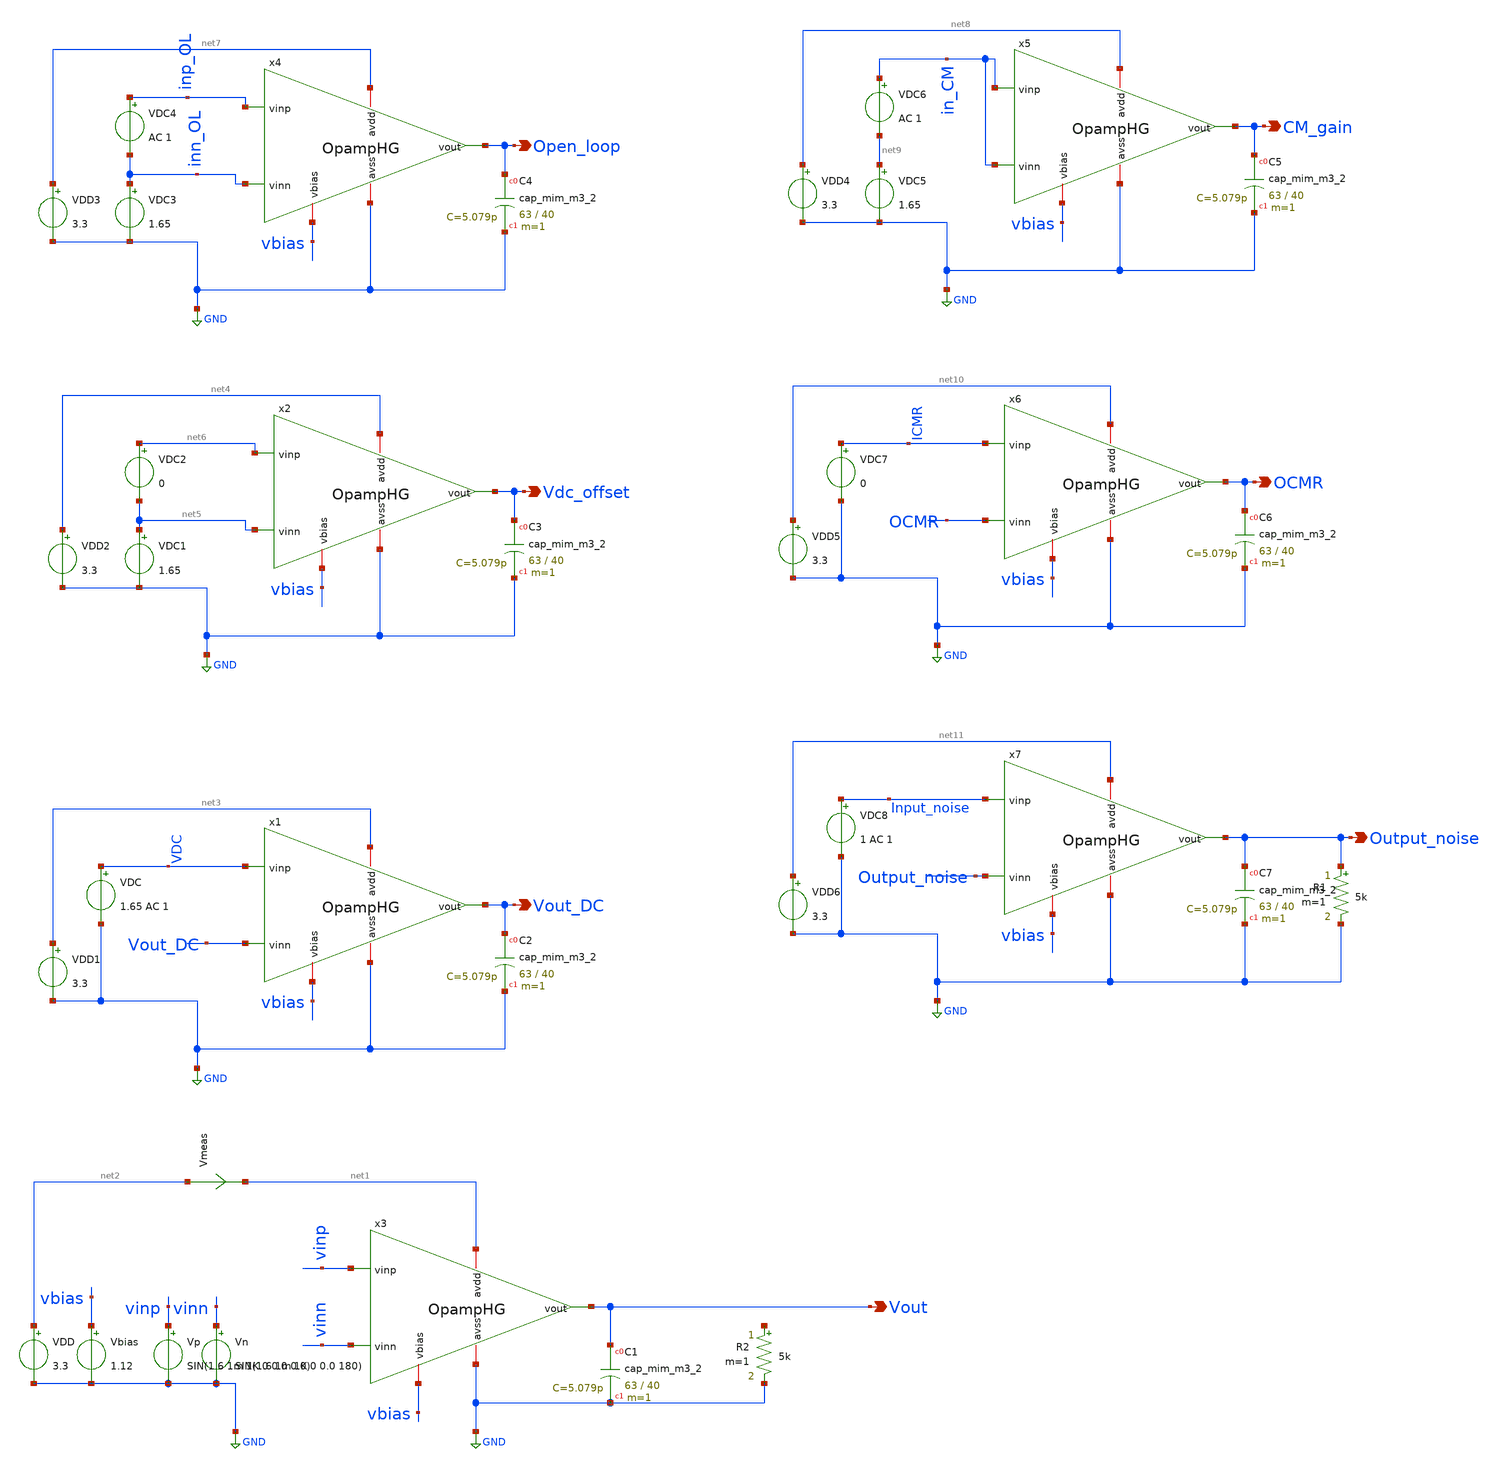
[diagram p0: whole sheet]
** sch_path: OpampHG_tb.sch
**.subckt OpampHG_tb Vout Vout_DC Vdc_offset Open_loop CM_gain OCMR Output_noise
*.opin Vout
*.opin Vout_DC
*.opin Vdc_offset
*.opin Open_loop
*.opin CM_gain
*.opin OCMR
*.opin Output_noise
Vp vinp GND SIN(1.6 1m 1K 0 0.0 0.0)
Vn vinn GND SIN(1.6 1m 1K 0 0.0 180)
VDD net2 GND 3.3
Vbias vbias GND 1.12
XC1 Vout GND sky130_fd_pr__cap_mim_m3_2 W=63 L=40 MF=1 m=1
x3 net1 GND vbias vinp vinn Vout OpampHG
x1 net3 GND vbias VDC Vout_DC Vout_DC OpampHG
VDD1 net3 GND 3.3
VDC VDC GND 1.65 AC 1
XC2 Vout_DC GND sky130_fd_pr__cap_mim_m3_2 W=63 L=40 MF=1 m=1
R1 Output_noise GND 5k m=1
x2 net4 GND vbias net6 net5 Vdc_offset OpampHG
VDD2 net4 GND 3.3
VDC1 net5 GND 1.65
XC3 Vdc_offset GND sky130_fd_pr__cap_mim_m3_2 W=63 L=40 MF=1 m=1
VDC2 net6 net5 0
x4 net7 GND vbias inp_OL inn_OL Open_loop OpampHG
VDD3 net7 GND 3.3
VDC3 inn_OL GND 1.65
XC4 Open_loop GND sky130_fd_pr__cap_mim_m3_2 W=63 L=40 MF=1 m=1
VDC4 inp_OL inn_OL AC 1
x5 net8 GND vbias in_CM in_CM CM_gain OpampHG
VDD4 net8 GND 3.3
VDC5 net9 GND 1.65
XC5 CM_gain GND sky130_fd_pr__cap_mim_m3_2 W=63 L=40 MF=1 m=1
VDC6 in_CM net9 AC 1
x6 net10 GND vbias ICMR OCMR OCMR OpampHG
VDD5 net10 GND 3.3
VDC7 ICMR GND 0
XC6 OCMR GND sky130_fd_pr__cap_mim_m3_2 W=63 L=40 MF=1 m=1
x7 net11 GND vbias Input_noise Output_noise Output_noise OpampHG
VDD6 net11 GND 3.3
VDC8 Input_noise GND 1 AC 1
XC7 Output_noise GND sky130_fd_pr__cap_mim_m3_2 W=63 L=40 MF=1 m=1
R2 net12 GND 5k m=1
Vmeas net2 net1 0
.save i(vmeas)
**** begin user architecture code


.lib /foss/pdks/sky130A/libs.tech/ngspice/sky130.lib.spice tt
.control

*****************dc analysis************
*dc VDC7 0 3.3 0.1
*plot v(OCMR) v(ICMR)
*dc VDC2 -5m 5m 1m
*plot v(Vdc_offset)


*****************AC analysis************
ac dec 20 1 1e10
let Open_Loop_Gain = v(Open_loop)/(v(inp_OL)-v(inn_OL))
let Common_mode_gain = v(CM_gain)/v(in_CM)
let Phase_Degree=180*cph(v(Open_loop)/(v(inp_OL)-v(inn_OL)))/pi
let CMRR=Open_Loop_Gain/Common_mode_gain
plot v(Vout_DC)
plot db(Open_Loop_Gain)
plot Phase_Degree
plot db(CMRR)
write Output_AC.raw

****************Transient Analysis******
*tran 0.1m 5m
*plot v(vinp) v(vinn)
*plot v(Vout)
*plot v(x3.vout_prior)
*write Output_tran.raw

*****************Noise Analysis**********
*noise v(Output_noise, 0) VDC8 dec 10 1 1e7
*setplot noise1
*write noise1.raw


.endc


**** end user architecture code
**.ends

* expanding   symbol:  /foss/designs/Opamp_HG/OpampHG.sym # of pins=6
** sym_path: OpampHG.sym
** sch_path: OpampHG.sch
.subckt OpampHG avdd avss vbias vinp vinn vout
*.iopin avdd
*.iopin avss
*.iopin vbias
*.ipin vinp
*.ipin vinn
*.opin vout
XC1 net2 Vout_prior sky130_fd_pr__cap_mim_m3_1 W=13 L=9.9 MF=1 m=1
XC2 net3 vout sky130_fd_pr__cap_mim_m3_2 W=20 L=37 MF=1 m=1
XM1 net1 net2 avdd avdd sky130_fd_pr__pfet_01v8 L=0.3 W=5 nf=1 ad='int((nf+1)/2) * W/nf * 0.29' as='int((nf+2)/2) * W/nf * 0.29'
+ pd='2*int((nf+1)/2) * (W/nf + 0.29)' ps='2*int((nf+2)/2) * (W/nf + 0.29)' nrd='0.29 / W' nrs='0.29 / W'
+ sa=0 sb=0 sd=0 mult=1 m=1
XM2 net3 net2 avdd avdd sky130_fd_pr__pfet_01v8 L=0.3 W=5 nf=1 ad='int((nf+1)/2) * W/nf * 0.29' as='int((nf+2)/2) * W/nf * 0.29'
+ pd='2*int((nf+1)/2) * (W/nf + 0.29)' ps='2*int((nf+2)/2) * (W/nf + 0.29)' nrd='0.29 / W' nrs='0.29 / W'
+ sa=0 sb=0 sd=0 mult=1 m=1
XM3 net2 net2 net1 avdd sky130_fd_pr__pfet_01v8 L=0.3 W=5 nf=1 ad='int((nf+1)/2) * W/nf * 0.29' as='int((nf+2)/2) * W/nf * 0.29'
+ pd='2*int((nf+1)/2) * (W/nf + 0.29)' ps='2*int((nf+2)/2) * (W/nf + 0.29)' nrd='0.29 / W' nrs='0.29 / W'
+ sa=0 sb=0 sd=0 mult=1 m=1
XM4 net5 net2 net3 avdd sky130_fd_pr__pfet_01v8 L=0.3 W=5 nf=1 ad='int((nf+1)/2) * W/nf * 0.29' as='int((nf+2)/2) * W/nf * 0.29'
+ pd='2*int((nf+1)/2) * (W/nf + 0.29)' ps='2*int((nf+2)/2) * (W/nf + 0.29)' nrd='0.29 / W' nrs='0.29 / W'
+ sa=0 sb=0 sd=0 mult=1 m=1
XM5 net7 net6 avdd avdd sky130_fd_pr__pfet_01v8 L=0.3 W=5 nf=1 ad='int((nf+1)/2) * W/nf * 0.29' as='int((nf+2)/2) * W/nf * 0.29'
+ pd='2*int((nf+1)/2) * (W/nf + 0.29)' ps='2*int((nf+2)/2) * (W/nf + 0.29)' nrd='0.29 / W' nrs='0.29 / W'
+ sa=0 sb=0 sd=0 mult=1 m=1
XM6 net8 net6 avdd avdd sky130_fd_pr__pfet_01v8 L=0.3 W=5 nf=1 ad='int((nf+1)/2) * W/nf * 0.29' as='int((nf+2)/2) * W/nf * 0.29'
+ pd='2*int((nf+1)/2) * (W/nf + 0.29)' ps='2*int((nf+2)/2) * (W/nf + 0.29)' nrd='0.29 / W' nrs='0.29 / W'
+ sa=0 sb=0 sd=0 mult=1 m=1
XM7 net6 net6 net7 avdd sky130_fd_pr__pfet_01v8 L=0.3 W=5 nf=1 ad='int((nf+1)/2) * W/nf * 0.29' as='int((nf+2)/2) * W/nf * 0.29'
+ pd='2*int((nf+1)/2) * (W/nf + 0.29)' ps='2*int((nf+2)/2) * (W/nf + 0.29)' nrd='0.29 / W' nrs='0.29 / W'
+ sa=0 sb=0 sd=0 mult=1 m=1
XM8 Vout_prior net6 net8 avdd sky130_fd_pr__pfet_01v8 L=0.3 W=5 nf=1 ad='int((nf+1)/2) * W/nf * 0.29'
+ as='int((nf+2)/2) * W/nf * 0.29' pd='2*int((nf+1)/2) * (W/nf + 0.29)' ps='2*int((nf+2)/2) * (W/nf + 0.29)'
+ nrd='0.29 / W' nrs='0.29 / W' sa=0 sb=0 sd=0 mult=1 m=1
XM9 net11 Vout_prior avdd avdd sky130_fd_pr__pfet_01v8 L=0.3 W=50 nf=1 ad='int((nf+1)/2) * W/nf * 0.29'
+ as='int((nf+2)/2) * W/nf * 0.29' pd='2*int((nf+1)/2) * (W/nf + 0.29)' ps='2*int((nf+2)/2) * (W/nf + 0.29)'
+ nrd='0.29 / W' nrs='0.29 / W' sa=0 sb=0 sd=0 mult=1 m=1
XM10 vout Vout_prior net11 avdd sky130_fd_pr__pfet_01v8 L=0.3 W=50 nf=1 ad='int((nf+1)/2) * W/nf * 0.29'
+ as='int((nf+2)/2) * W/nf * 0.29' pd='2*int((nf+1)/2) * (W/nf + 0.29)' ps='2*int((nf+2)/2) * (W/nf + 0.29)'
+ nrd='0.29 / W' nrs='0.29 / W' sa=0 sb=0 sd=0 mult=1 m=1
XM11 net2 vinn net4 avss sky130_fd_pr__nfet_01v8 L=2 W=5 nf=1 ad='int((nf+1)/2) * W/nf * 0.29' as='int((nf+2)/2) * W/nf * 0.29'
+ pd='2*int((nf+1)/2) * (W/nf + 0.29)' ps='2*int((nf+2)/2) * (W/nf + 0.29)' nrd='0.29 / W' nrs='0.29 / W'
+ sa=0 sb=0 sd=0 mult=1 m=1
XM12 net5 vinp net4 avss sky130_fd_pr__nfet_01v8 L=2 W=5 nf=1 ad='int((nf+1)/2) * W/nf * 0.29' as='int((nf+2)/2) * W/nf * 0.29'
+ pd='2*int((nf+1)/2) * (W/nf + 0.29)' ps='2*int((nf+2)/2) * (W/nf + 0.29)' nrd='0.29 / W' nrs='0.29 / W'
+ sa=0 sb=0 sd=0 mult=1 m=1
XM13 net6 net5 net10 avss sky130_fd_pr__nfet_01v8 L=2 W=5 nf=1 ad='int((nf+1)/2) * W/nf * 0.29' as='int((nf+2)/2) * W/nf * 0.29'
+ pd='2*int((nf+1)/2) * (W/nf + 0.29)' ps='2*int((nf+2)/2) * (W/nf + 0.29)' nrd='0.29 / W' nrs='0.29 / W'
+ sa=0 sb=0 sd=0 mult=1 m=1
XM14 Vout_prior net2 net9 avss sky130_fd_pr__nfet_01v8 L=2 W=5 nf=1 ad='int((nf+1)/2) * W/nf * 0.29'
+ as='int((nf+2)/2) * W/nf * 0.29' pd='2*int((nf+1)/2) * (W/nf + 0.29)' ps='2*int((nf+2)/2) * (W/nf + 0.29)'
+ nrd='0.29 / W' nrs='0.29 / W' sa=0 sb=0 sd=0 mult=1 m=1
XM15 net4 vbias avss avss sky130_fd_pr__nfet_01v8 L=0.6 W=2.6 nf=1 ad='int((nf+1)/2) * W/nf * 0.29' as='int((nf+2)/2) * W/nf * 0.29'
+ pd='2*int((nf+1)/2) * (W/nf + 0.29)' ps='2*int((nf+2)/2) * (W/nf + 0.29)' nrd='0.29 / W' nrs='0.29 / W'
+ sa=0 sb=0 sd=0 mult=1 m=1
XM16 net4 vbias avss avss sky130_fd_pr__nfet_01v8 L=0.6 W=2.6 nf=1 ad='int((nf+1)/2) * W/nf * 0.29' as='int((nf+2)/2) * W/nf * 0.29'
+ pd='2*int((nf+1)/2) * (W/nf + 0.29)' ps='2*int((nf+2)/2) * (W/nf + 0.29)' nrd='0.29 / W' nrs='0.29 / W'
+ sa=0 sb=0 sd=0 mult=1 m=1
XM17 net10 vbias avss avss sky130_fd_pr__nfet_01v8 L=0.6 W=2.6 nf=1 ad='int((nf+1)/2) * W/nf * 0.29'
+ as='int((nf+2)/2) * W/nf * 0.29' pd='2*int((nf+1)/2) * (W/nf + 0.29)' ps='2*int((nf+2)/2) * (W/nf + 0.29)'
+ nrd='0.29 / W' nrs='0.29 / W' sa=0 sb=0 sd=0 mult=1 m=1
XM18 net9 vbias avss avss sky130_fd_pr__nfet_01v8 L=0.6 W=2.6 nf=1 ad='int((nf+1)/2) * W/nf * 0.29' as='int((nf+2)/2) * W/nf * 0.29'
+ pd='2*int((nf+1)/2) * (W/nf + 0.29)' ps='2*int((nf+2)/2) * (W/nf + 0.29)' nrd='0.29 / W' nrs='0.29 / W'
+ sa=0 sb=0 sd=0 mult=1 m=1
XM19 vout vbias avss avss sky130_fd_pr__nfet_01v8 L=0.6 W=20.4 nf=1 ad='int((nf+1)/2) * W/nf * 0.29'
+ as='int((nf+2)/2) * W/nf * 0.29' pd='2*int((nf+1)/2) * (W/nf + 0.29)' ps='2*int((nf+2)/2) * (W/nf + 0.29)'
+ nrd='0.29 / W' nrs='0.29 / W' sa=0 sb=0 sd=0 mult=1 m=1
.ends

.GLOBAL GND
.end
